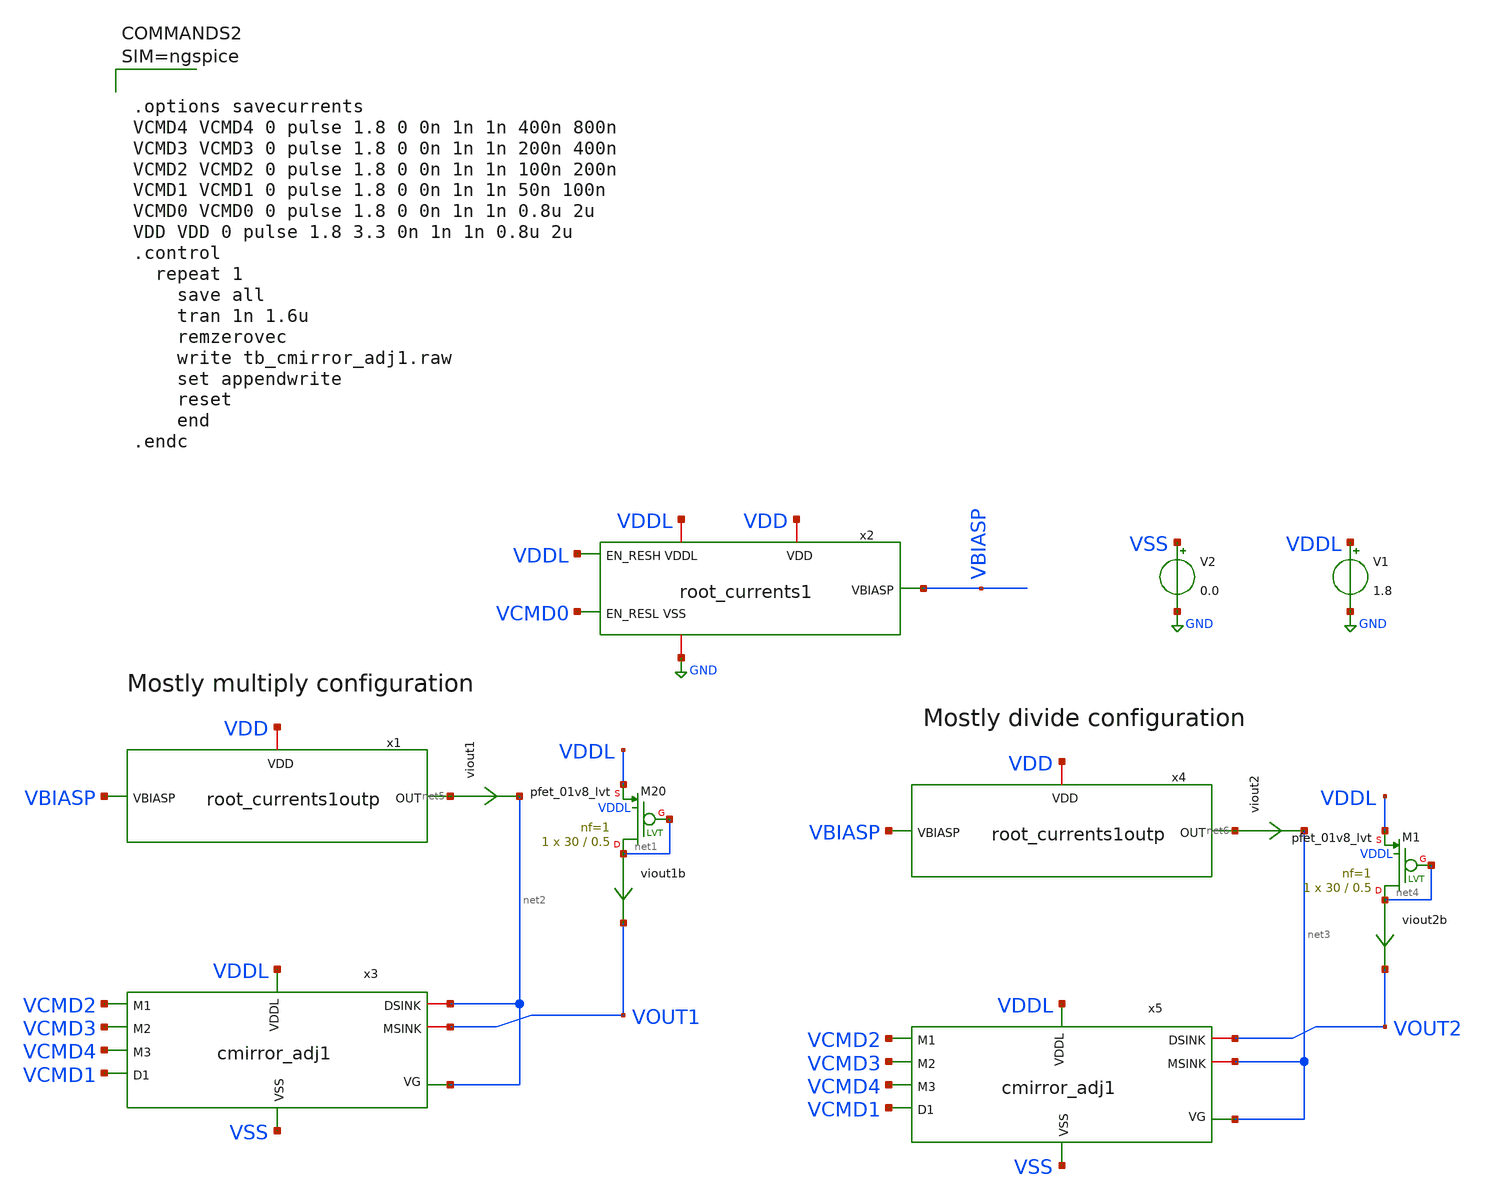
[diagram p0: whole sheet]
** sch_path: xschem/tb_cmirror_adj1.sch
**.subckt tb_cmirror_adj1
x2 VDDL VCMD0 VBIASP VDD VDDL GND root_currents1
V1 VDDL GND 1.8
x1 VBIASP net5 VDD root_currents1outp
viout1 net5 net2 0
.save i(viout1)
V2 VSS GND 0.0
viout1b net1 VOUT1 0
.save i(viout1b)
XM20 net1 net1 VDDL VDDL sky130_fd_pr__pfet_01v8_lvt L=0.5 W=30 nf=1 ad='int((nf+1)/2) * W/nf * 0.29'
+ as='int((nf+2)/2) * W/nf * 0.29' pd='2*int((nf+1)/2) * (W/nf + 0.29)' ps='2*int((nf+2)/2) * (W/nf + 0.29)'
+ nrd='0.29 / W' nrs='0.29 / W' sa=0 sb=0 sd=0 mult=1 m=1
x3 VCMD2 VCMD3 VCMD4 VCMD1 VDDL VSS net2 net2 VOUT1 cmirror_adj1
x4 VBIASP net6 VDD root_currents1outp
viout2 net6 net3 0
.save i(viout2)
x5 VCMD2 VCMD3 VCMD4 VCMD1 VDDL VSS net3 VOUT2 net3 cmirror_adj1
viout2b net4 VOUT2 0
.save i(viout2b)
XM1 net4 net4 VDDL VDDL sky130_fd_pr__pfet_01v8_lvt L=0.5 W=30 nf=1 ad='int((nf+1)/2) * W/nf * 0.29'
+ as='int((nf+2)/2) * W/nf * 0.29' pd='2*int((nf+1)/2) * (W/nf + 0.29)' ps='2*int((nf+2)/2) * (W/nf + 0.29)'
+ nrd='0.29 / W' nrs='0.29 / W' sa=0 sb=0 sd=0 mult=1 m=1
**** begin user architecture code

** opencircuitdesign pdks install
.lib $::SKYWATER_MODELS/sky130.lib.spice tt





.options savecurrents
VCMD4 VCMD4 0 pulse 1.8 0 0n 1n 1n 400n 800n
VCMD3 VCMD3 0 pulse 1.8 0 0n 1n 1n 200n 400n
VCMD2 VCMD2 0 pulse 1.8 0 0n 1n 1n 100n 200n
VCMD1 VCMD1 0 pulse 1.8 0 0n 1n 1n 50n 100n
VCMD0 VCMD0 0 pulse 1.8 0 0n 1n 1n 0.8u 2u
VDD VDD 0 pulse 1.8 3.3 0n 1n 1n 0.8u 2u
.control
  repeat 1
    save all
    tran 1n 1.6u
    remzerovec
    write tb_cmirror_adj1.raw
    set appendwrite
    reset
    end
.endc



**** end user architecture code
**.ends

* expanding   symbol:  root_currents1.sym # of pins=6
** sym_path: xschem/root_currents1.sym
** sch_path: xschem/root_currents1.sch
.subckt root_currents1 EN_RESH EN_RESL VBIASP VDD VDDL VSS
*.iopin VSS
*.ipin EN_RESH
*.opin VBIASP
*.iopin VDDL
*.iopin VDD
*.ipin EN_RESL
XR1 V1 net2 net4 sky130_fd_pr__res_high_po_0p35 L=20 mult=1 m=1
XR2 V2 net3 net5 sky130_fd_pr__res_high_po_0p69 L=8 mult=1 m=1
XM4 VMID VMID VSS VSS sky130_fd_pr__nfet_01v8_lvt L=0.5 W=4 nf=1 ad='int((nf+1)/2) * W/nf * 0.29' as='int((nf+2)/2) * W/nf * 0.29'
+ pd='2*int((nf+1)/2) * (W/nf + 0.29)' ps='2*int((nf+2)/2) * (W/nf + 0.29)' nrd='0.29 / W' nrs='0.29 / W'
+ sa=0 sb=0 sd=0 mult=1 m=1
XM5 VMID VMID VSS VSS sky130_fd_pr__nfet_01v8_lvt L=0.5 W=4 nf=1 ad='int((nf+1)/2) * W/nf * 0.29' as='int((nf+2)/2) * W/nf * 0.29'
+ pd='2*int((nf+1)/2) * (W/nf + 0.29)' ps='2*int((nf+2)/2) * (W/nf + 0.29)' nrd='0.29 / W' nrs='0.29 / W'
+ sa=0 sb=0 sd=0 mult=1 m=1
XM6 net1 VMID VSS VSS sky130_fd_pr__nfet_01v8_lvt L=0.5 W=4 nf=1 ad='int((nf+1)/2) * W/nf * 0.29' as='int((nf+2)/2) * W/nf * 0.29'
+ pd='2*int((nf+1)/2) * (W/nf + 0.29)' ps='2*int((nf+2)/2) * (W/nf + 0.29)' nrd='0.29 / W' nrs='0.29 / W'
+ sa=0 sb=0 sd=0 mult=1 m=1
XM2 V1 EN_RESH_VDD VMID VSS sky130_fd_pr__nfet_g5v0d10v5 L=0.5 W=4 nf=1 ad='int((nf+1)/2) * W/nf * 0.29'
+ as='int((nf+2)/2) * W/nf * 0.29' pd='2*int((nf+1)/2) * (W/nf + 0.29)' ps='2*int((nf+2)/2) * (W/nf + 0.29)'
+ nrd='0.29 / W' nrs='0.29 / W' sa=0 sb=0 sd=0 mult=1 m=1
viout VBIASP net1 0
.save i(viout)
x1 EN_RESH EN_RESH_VDD net6 VDD VDDL VSS lvl_shift_lohi1
XM7 VBIASP VBIASP VDD VDD sky130_fd_pr__pfet_g5v0d10v5 L=0.5 W=4 nf=1 ad='int((nf+1)/2) * W/nf * 0.29'
+ as='int((nf+2)/2) * W/nf * 0.29' pd='2*int((nf+1)/2) * (W/nf + 0.29)' ps='2*int((nf+2)/2) * (W/nf + 0.29)'
+ nrd='0.29 / W' nrs='0.29 / W' sa=0 sb=0 sd=0 mult=1 m=1
vin1 VDD net2 0
.save i(vin1)
vin2 VDDL net3 0
.save i(vin2)
XM1 V2 EN_RESL VMID VSS sky130_fd_pr__nfet_01v8_lvt L=0.5 W=4 nf=1 ad='int((nf+1)/2) * W/nf * 0.29' as='int((nf+2)/2) * W/nf * 0.29'
+ pd='2*int((nf+1)/2) * (W/nf + 0.29)' ps='2*int((nf+2)/2) * (W/nf + 0.29)' nrd='0.29 / W' nrs='0.29 / W'
+ sa=0 sb=0 sd=0 mult=1 m=1
.ends


* expanding   symbol:  root_currents1outp.sym # of pins=3
** sym_path: xschem/root_currents1outp.sym
** sch_path: xschem/root_currents1outp.sch
.subckt root_currents1outp VBIASP OUT VDD
*.iopin VBIASP
*.iopin OUT
*.iopin VDD
XM7 net1 VBIASP VDD VDD sky130_fd_pr__pfet_g5v0d10v5 L=0.5 W=4 nf=1 ad='int((nf+1)/2) * W/nf * 0.29'
+ as='int((nf+2)/2) * W/nf * 0.29' pd='2*int((nf+1)/2) * (W/nf + 0.29)' ps='2*int((nf+2)/2) * (W/nf + 0.29)'
+ nrd='0.29 / W' nrs='0.29 / W' sa=0 sb=0 sd=0 mult=1 m=1
viout net1 OUT 0
.save i(viout)
.ends


* expanding   symbol:  cmirror_adj1.sym # of pins=9
** sym_path: xschem/cmirror_adj1.sym
** sch_path: xschem/cmirror_adj1.sch
.subckt cmirror_adj1 M1 M2 M3 D1 VDDL VSS VG DSINK MSINK
*.ipin VSS
*.ipin VG
*.ipin VDDL
*.iopin MSINK
*.ipin M3
*.ipin M2
*.ipin M1
*.iopin DSINK
*.ipin D1
XM1 net1 D1 VSS VSS sky130_fd_pr__nfet_01v8_lvt L=0.3 W=0.5 nf=1 ad='int((nf+1)/2) * W/nf * 0.29' as='int((nf+2)/2) * W/nf * 0.29'
+ pd='2*int((nf+1)/2) * (W/nf + 0.29)' ps='2*int((nf+2)/2) * (W/nf + 0.29)' nrd='0.29 / W' nrs='0.29 / W'
+ sa=0 sb=0 sd=0 mult=1 m=1
XM2 net2 VG net1 VSS sky130_fd_pr__nfet_01v8_lvt L=0.3 W=0.5 nf=1 ad='int((nf+1)/2) * W/nf * 0.29' as='int((nf+2)/2) * W/nf * 0.29'
+ pd='2*int((nf+1)/2) * (W/nf + 0.29)' ps='2*int((nf+2)/2) * (W/nf + 0.29)' nrd='0.29 / W' nrs='0.29 / W'
+ sa=0 sb=0 sd=0 mult=1 m=1
XM10 net3 VDDL VSS VSS sky130_fd_pr__nfet_01v8_lvt L=0.3 W=0.5 nf=1 ad='int((nf+1)/2) * W/nf * 0.29'
+ as='int((nf+2)/2) * W/nf * 0.29' pd='2*int((nf+1)/2) * (W/nf + 0.29)' ps='2*int((nf+2)/2) * (W/nf + 0.29)'
+ nrd='0.29 / W' nrs='0.29 / W' sa=0 sb=0 sd=0 mult=1 m=1
XM11 net2 VG net3 VSS sky130_fd_pr__nfet_01v8_lvt L=0.3 W=0.5 nf=1 ad='int((nf+1)/2) * W/nf * 0.29' as='int((nf+2)/2) * W/nf * 0.29'
+ pd='2*int((nf+1)/2) * (W/nf + 0.29)' ps='2*int((nf+2)/2) * (W/nf + 0.29)' nrd='0.29 / W' nrs='0.29 / W'
+ sa=0 sb=0 sd=0 mult=1 m=1
XM3 net4 M1 VSS VSS sky130_fd_pr__nfet_01v8_lvt L=0.3 W=0.5 nf=1 ad='int((nf+1)/2) * W/nf * 0.29' as='int((nf+2)/2) * W/nf * 0.29'
+ pd='2*int((nf+1)/2) * (W/nf + 0.29)' ps='2*int((nf+2)/2) * (W/nf + 0.29)' nrd='0.29 / W' nrs='0.29 / W'
+ sa=0 sb=0 sd=0 mult=1 m=1
XM4 MSINK VG net4 VSS sky130_fd_pr__nfet_01v8_lvt L=0.3 W=0.5 nf=1 ad='int((nf+1)/2) * W/nf * 0.29' as='int((nf+2)/2) * W/nf * 0.29'
+ pd='2*int((nf+1)/2) * (W/nf + 0.29)' ps='2*int((nf+2)/2) * (W/nf + 0.29)' nrd='0.29 / W' nrs='0.29 / W'
+ sa=0 sb=0 sd=0 mult=1 m=1
XM5 net5 M2 VSS VSS sky130_fd_pr__nfet_01v8_lvt L=0.3 W=0.5 nf=1 ad='int((nf+1)/2) * W/nf * 0.29' as='int((nf+2)/2) * W/nf * 0.29'
+ pd='2*int((nf+1)/2) * (W/nf + 0.29)' ps='2*int((nf+2)/2) * (W/nf + 0.29)' nrd='0.29 / W' nrs='0.29 / W'
+ sa=0 sb=0 sd=0 mult=1 m=1
XM6 MSINK VG net5 VSS sky130_fd_pr__nfet_01v8_lvt L=0.3 W=0.5 nf=1 ad='int((nf+1)/2) * W/nf * 0.29' as='int((nf+2)/2) * W/nf * 0.29'
+ pd='2*int((nf+1)/2) * (W/nf + 0.29)' ps='2*int((nf+2)/2) * (W/nf + 0.29)' nrd='0.29 / W' nrs='0.29 / W'
+ sa=0 sb=0 sd=0 mult=1 m=1
XM8 net6 M2 VSS VSS sky130_fd_pr__nfet_01v8_lvt L=0.3 W=0.5 nf=1 ad='int((nf+1)/2) * W/nf * 0.29' as='int((nf+2)/2) * W/nf * 0.29'
+ pd='2*int((nf+1)/2) * (W/nf + 0.29)' ps='2*int((nf+2)/2) * (W/nf + 0.29)' nrd='0.29 / W' nrs='0.29 / W'
+ sa=0 sb=0 sd=0 mult=1 m=1
XM9 MSINK VG net6 VSS sky130_fd_pr__nfet_01v8_lvt L=0.3 W=0.5 nf=1 ad='int((nf+1)/2) * W/nf * 0.29' as='int((nf+2)/2) * W/nf * 0.29'
+ pd='2*int((nf+1)/2) * (W/nf + 0.29)' ps='2*int((nf+2)/2) * (W/nf + 0.29)' nrd='0.29 / W' nrs='0.29 / W'
+ sa=0 sb=0 sd=0 mult=1 m=1
XM12 net7 M3 VSS VSS sky130_fd_pr__nfet_01v8_lvt L=0.3 W=0.5 nf=1 ad='int((nf+1)/2) * W/nf * 0.29' as='int((nf+2)/2) * W/nf * 0.29'
+ pd='2*int((nf+1)/2) * (W/nf + 0.29)' ps='2*int((nf+2)/2) * (W/nf + 0.29)' nrd='0.29 / W' nrs='0.29 / W'
+ sa=0 sb=0 sd=0 mult=1 m=1
XM13 MSINK VG net7 VSS sky130_fd_pr__nfet_01v8_lvt L=0.3 W=0.5 nf=1 ad='int((nf+1)/2) * W/nf * 0.29'
+ as='int((nf+2)/2) * W/nf * 0.29' pd='2*int((nf+1)/2) * (W/nf + 0.29)' ps='2*int((nf+2)/2) * (W/nf + 0.29)'
+ nrd='0.29 / W' nrs='0.29 / W' sa=0 sb=0 sd=0 mult=1 m=1
XM14 net8 M3 VSS VSS sky130_fd_pr__nfet_01v8_lvt L=0.3 W=0.5 nf=1 ad='int((nf+1)/2) * W/nf * 0.29' as='int((nf+2)/2) * W/nf * 0.29'
+ pd='2*int((nf+1)/2) * (W/nf + 0.29)' ps='2*int((nf+2)/2) * (W/nf + 0.29)' nrd='0.29 / W' nrs='0.29 / W'
+ sa=0 sb=0 sd=0 mult=1 m=1
XM15 MSINK VG net8 VSS sky130_fd_pr__nfet_01v8_lvt L=0.3 W=0.5 nf=1 ad='int((nf+1)/2) * W/nf * 0.29'
+ as='int((nf+2)/2) * W/nf * 0.29' pd='2*int((nf+1)/2) * (W/nf + 0.29)' ps='2*int((nf+2)/2) * (W/nf + 0.29)'
+ nrd='0.29 / W' nrs='0.29 / W' sa=0 sb=0 sd=0 mult=1 m=1
XM16 net9 M3 VSS VSS sky130_fd_pr__nfet_01v8_lvt L=0.3 W=0.5 nf=1 ad='int((nf+1)/2) * W/nf * 0.29' as='int((nf+2)/2) * W/nf * 0.29'
+ pd='2*int((nf+1)/2) * (W/nf + 0.29)' ps='2*int((nf+2)/2) * (W/nf + 0.29)' nrd='0.29 / W' nrs='0.29 / W'
+ sa=0 sb=0 sd=0 mult=1 m=1
XM17 MSINK VG net9 VSS sky130_fd_pr__nfet_01v8_lvt L=0.3 W=0.5 nf=1 ad='int((nf+1)/2) * W/nf * 0.29'
+ as='int((nf+2)/2) * W/nf * 0.29' pd='2*int((nf+1)/2) * (W/nf + 0.29)' ps='2*int((nf+2)/2) * (W/nf + 0.29)'
+ nrd='0.29 / W' nrs='0.29 / W' sa=0 sb=0 sd=0 mult=1 m=1
XM18 net10 M3 VSS VSS sky130_fd_pr__nfet_01v8_lvt L=0.3 W=0.5 nf=1 ad='int((nf+1)/2) * W/nf * 0.29' as='int((nf+2)/2) * W/nf * 0.29'
+ pd='2*int((nf+1)/2) * (W/nf + 0.29)' ps='2*int((nf+2)/2) * (W/nf + 0.29)' nrd='0.29 / W' nrs='0.29 / W'
+ sa=0 sb=0 sd=0 mult=1 m=1
XM19 MSINK VG net10 VSS sky130_fd_pr__nfet_01v8_lvt L=0.3 W=0.5 nf=1 ad='int((nf+1)/2) * W/nf * 0.29'
+ as='int((nf+2)/2) * W/nf * 0.29' pd='2*int((nf+1)/2) * (W/nf + 0.29)' ps='2*int((nf+2)/2) * (W/nf + 0.29)'
+ nrd='0.29 / W' nrs='0.29 / W' sa=0 sb=0 sd=0 mult=1 m=1
XM7 net11 D1 VSS VSS sky130_fd_pr__nfet_01v8_lvt L=0.3 W=0.5 nf=1 ad='int((nf+1)/2) * W/nf * 0.29' as='int((nf+2)/2) * W/nf * 0.29'
+ pd='2*int((nf+1)/2) * (W/nf + 0.29)' ps='2*int((nf+2)/2) * (W/nf + 0.29)' nrd='0.29 / W' nrs='0.29 / W'
+ sa=0 sb=0 sd=0 mult=1 m=1
XM21 net2 VG net11 VSS sky130_fd_pr__nfet_01v8_lvt L=0.3 W=0.5 nf=1 ad='int((nf+1)/2) * W/nf * 0.29'
+ as='int((nf+2)/2) * W/nf * 0.29' pd='2*int((nf+1)/2) * (W/nf + 0.29)' ps='2*int((nf+2)/2) * (W/nf + 0.29)'
+ nrd='0.29 / W' nrs='0.29 / W' sa=0 sb=0 sd=0 mult=1 m=1
XM22 net12 VDDL VSS VSS sky130_fd_pr__nfet_01v8_lvt L=0.3 W=0.5 nf=1 ad='int((nf+1)/2) * W/nf * 0.29'
+ as='int((nf+2)/2) * W/nf * 0.29' pd='2*int((nf+1)/2) * (W/nf + 0.29)' ps='2*int((nf+2)/2) * (W/nf + 0.29)'
+ nrd='0.29 / W' nrs='0.29 / W' sa=0 sb=0 sd=0 mult=1 m=1
XM23 MSINK VG net12 VSS sky130_fd_pr__nfet_01v8_lvt L=0.3 W=0.5 nf=1 ad='int((nf+1)/2) * W/nf * 0.29'
+ as='int((nf+2)/2) * W/nf * 0.29' pd='2*int((nf+1)/2) * (W/nf + 0.29)' ps='2*int((nf+2)/2) * (W/nf + 0.29)'
+ nrd='0.29 / W' nrs='0.29 / W' sa=0 sb=0 sd=0 mult=1 m=1
vidsink DSINK net2 0
.save i(vidsink)
.ends


* expanding   symbol:  lvl_shift_lohi1.sym # of pins=6
** sym_path: xschem/lvl_shift_lohi1.sym
** sch_path: xschem/lvl_shift_lohi1.sch
.subckt lvl_shift_lohi1 D Q QB VDDH VDDL VSS
*.ipin D
*.opin Q
*.opin QB
*.iopin VDDH
*.iopin VDDL
*.iopin VSS
vpwr VDDL net1 0
.save i(vpwr)
XM1 QB Q VDDH VDDH sky130_fd_pr__pfet_g5v0d10v5 L=0.5 W=2 nf=1 ad='int((nf+1)/2) * W/nf * 0.29' as='int((nf+2)/2) * W/nf * 0.29'
+ pd='2*int((nf+1)/2) * (W/nf + 0.29)' ps='2*int((nf+2)/2) * (W/nf + 0.29)' nrd='0.29 / W' nrs='0.29 / W'
+ sa=0 sb=0 sd=0 mult=1 m=1
XM2 Q QB VDDH VDDH sky130_fd_pr__pfet_g5v0d10v5 L=0.5 W=2 nf=1 ad='int((nf+1)/2) * W/nf * 0.29' as='int((nf+2)/2) * W/nf * 0.29'
+ pd='2*int((nf+1)/2) * (W/nf + 0.29)' ps='2*int((nf+2)/2) * (W/nf + 0.29)' nrd='0.29 / W' nrs='0.29 / W'
+ sa=0 sb=0 sd=0 mult=1 m=1
XM3 QB D VSS VSS sky130_fd_pr__nfet_g5v0d10v5 L=0.5 W=4 nf=1 ad='int((nf+1)/2) * W/nf * 0.29' as='int((nf+2)/2) * W/nf * 0.29'
+ pd='2*int((nf+1)/2) * (W/nf + 0.29)' ps='2*int((nf+2)/2) * (W/nf + 0.29)' nrd='0.29 / W' nrs='0.29 / W'
+ sa=0 sb=0 sd=0 mult=1 m=1
XM4 Q DB VSS VSS sky130_fd_pr__nfet_g5v0d10v5 L=0.5 W=4 nf=1 ad='int((nf+1)/2) * W/nf * 0.29' as='int((nf+2)/2) * W/nf * 0.29'
+ pd='2*int((nf+1)/2) * (W/nf + 0.29)' ps='2*int((nf+2)/2) * (W/nf + 0.29)' nrd='0.29 / W' nrs='0.29 / W'
+ sa=0 sb=0 sd=0 mult=1 m=1
XM5 DB D VSS VSS sky130_fd_pr__nfet_01v8_lvt L=0.5 W=1 nf=1 ad='int((nf+1)/2) * W/nf * 0.29' as='int((nf+2)/2) * W/nf * 0.29'
+ pd='2*int((nf+1)/2) * (W/nf + 0.29)' ps='2*int((nf+2)/2) * (W/nf + 0.29)' nrd='0.29 / W' nrs='0.29 / W'
+ sa=0 sb=0 sd=0 mult=1 m=1
XM6 DB D net1 VDDL sky130_fd_pr__pfet_01v8_lvt L=0.5 W=2 nf=1 ad='int((nf+1)/2) * W/nf * 0.29' as='int((nf+2)/2) * W/nf * 0.29'
+ pd='2*int((nf+1)/2) * (W/nf + 0.29)' ps='2*int((nf+2)/2) * (W/nf + 0.29)' nrd='0.29 / W' nrs='0.29 / W'
+ sa=0 sb=0 sd=0 mult=1 m=1
.ends

.GLOBAL GND
.end
